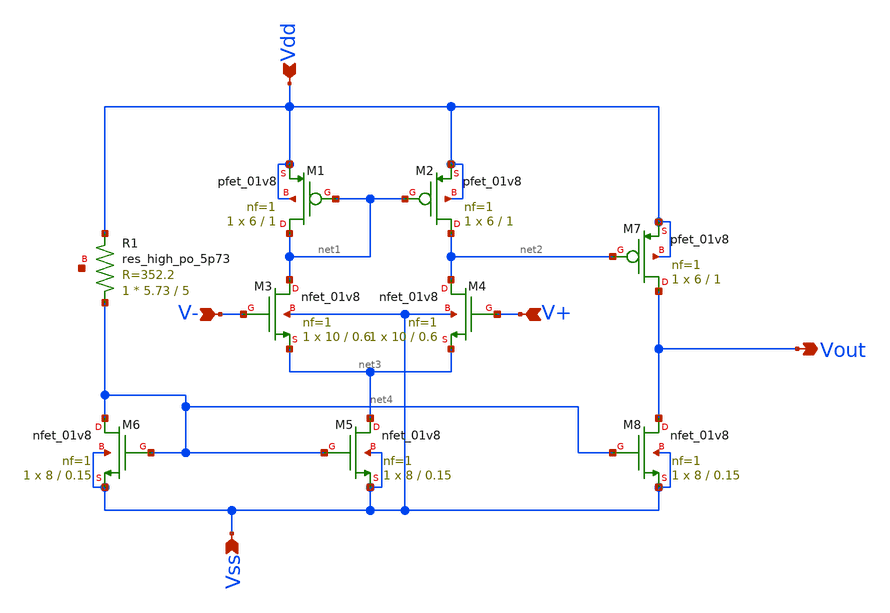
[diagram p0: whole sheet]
** sch_path: analog/schematics/opamp_single_stage.sch
**.subckt opamp_single_stage Vout Vdd Vss V+ V-
*.opin Vout
*.ipin Vdd
*.ipin Vss
*.ipin V+
*.ipin V-
XM3 net1 V- net3 Vss sky130_fd_pr__nfet_01v8 L=0.6 W=10 nf=1 ad='int((nf+1)/2) * W/nf * 0.29' as='int((nf+2)/2) * W/nf * 0.29'
+ pd='2*int((nf+1)/2) * (W/nf + 0.29)' ps='2*int((nf+2)/2) * (W/nf + 0.29)' nrd='0.29 / W' nrs='0.29 / W'
+ sa=0 sb=0 sd=0 mult=1 m=1
XM4 net2 V+ net3 Vss sky130_fd_pr__nfet_01v8 L=0.6 W=10 nf=1 ad='int((nf+1)/2) * W/nf * 0.29' as='int((nf+2)/2) * W/nf * 0.29'
+ pd='2*int((nf+1)/2) * (W/nf + 0.29)' ps='2*int((nf+2)/2) * (W/nf + 0.29)' nrd='0.29 / W' nrs='0.29 / W'
+ sa=0 sb=0 sd=0 mult=1 m=1
XM5 net3 net4 Vss Vss sky130_fd_pr__nfet_01v8 L=0.15 W=8 nf=1 ad='int((nf+1)/2) * W/nf * 0.29' as='int((nf+2)/2) * W/nf * 0.29'
+ pd='2*int((nf+1)/2) * (W/nf + 0.29)' ps='2*int((nf+2)/2) * (W/nf + 0.29)' nrd='0.29 / W' nrs='0.29 / W'
+ sa=0 sb=0 sd=0 mult=1 m=1
XM1 net1 net1 Vdd Vdd sky130_fd_pr__pfet_01v8 L=1 W=6 nf=1 ad='int((nf+1)/2) * W/nf * 0.29' as='int((nf+2)/2) * W/nf * 0.29'
+ pd='2*int((nf+1)/2) * (W/nf + 0.29)' ps='2*int((nf+2)/2) * (W/nf + 0.29)' nrd='0.29 / W' nrs='0.29 / W'
+ sa=0 sb=0 sd=0 mult=1 m=1
XM2 net2 net1 Vdd Vdd sky130_fd_pr__pfet_01v8 L=1 W=6 nf=1 ad='int((nf+1)/2) * W/nf * 0.29' as='int((nf+2)/2) * W/nf * 0.29'
+ pd='2*int((nf+1)/2) * (W/nf + 0.29)' ps='2*int((nf+2)/2) * (W/nf + 0.29)' nrd='0.29 / W' nrs='0.29 / W'
+ sa=0 sb=0 sd=0 mult=1 m=1
XM6 net4 net4 Vss Vss sky130_fd_pr__nfet_01v8 L=0.15 W=8 nf=1 ad='int((nf+1)/2) * W/nf * 0.29' as='int((nf+2)/2) * W/nf * 0.29'
+ pd='2*int((nf+1)/2) * (W/nf + 0.29)' ps='2*int((nf+2)/2) * (W/nf + 0.29)' nrd='0.29 / W' nrs='0.29 / W'
+ sa=0 sb=0 sd=0 mult=1 m=1
XM8 Vout net4 Vss Vss sky130_fd_pr__nfet_01v8 L=0.15 W=8 nf=1 ad='int((nf+1)/2) * W/nf * 0.29' as='int((nf+2)/2) * W/nf * 0.29'
+ pd='2*int((nf+1)/2) * (W/nf + 0.29)' ps='2*int((nf+2)/2) * (W/nf + 0.29)' nrd='0.29 / W' nrs='0.29 / W'
+ sa=0 sb=0 sd=0 mult=1 m=1
XM7 Vout net2 Vdd Vdd sky130_fd_pr__pfet_01v8 L=1 W=6 nf=1 ad='int((nf+1)/2) * W/nf * 0.29' as='int((nf+2)/2) * W/nf * 0.29'
+ pd='2*int((nf+1)/2) * (W/nf + 0.29)' ps='2*int((nf+2)/2) * (W/nf + 0.29)' nrd='0.29 / W' nrs='0.29 / W'
+ sa=0 sb=0 sd=0 mult=1 m=1
XR1 net4 Vdd net5 sky130_fd_pr__res_high_po_5p73 L=5 mult=1 m=1
**.ends
.end
